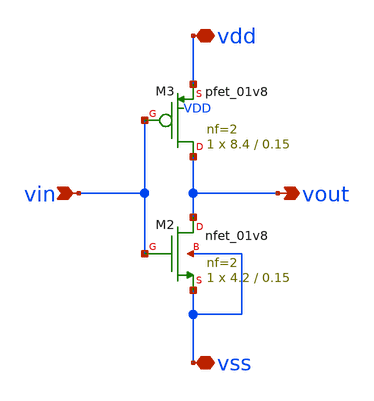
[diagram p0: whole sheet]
** sch_path: Week 0/xschem/inverter.sch
**.subckt inverter vin vout vdd vss
*.ipin vin
*.opin vout
*.iopin vdd
*.iopin vss
XM2 vout vin vss vss sky130_fd_pr__nfet_01v8 L=0.15 W=4.2 nf=2 ad='int((nf+1)/2) * W/nf * 0.29' as='int((nf+2)/2) * W/nf * 0.29'
+ pd='2*int((nf+1)/2) * (W/nf + 0.29)' ps='2*int((nf+2)/2) * (W/nf + 0.29)' nrd='0.29 / W' nrs='0.29 / W'
+ sa=0 sb=0 sd=0 mult=1 m=1
XM3 vout vin vdd VDD sky130_fd_pr__pfet_01v8 L=0.15 W=8.4 nf=2 ad='int((nf+1)/2) * W/nf * 0.29' as='int((nf+2)/2) * W/nf * 0.29'
+ pd='2*int((nf+1)/2) * (W/nf + 0.29)' ps='2*int((nf+2)/2) * (W/nf + 0.29)' nrd='0.29 / W' nrs='0.29 / W'
+ sa=0 sb=0 sd=0 mult=1 m=1
**.ends
.end
